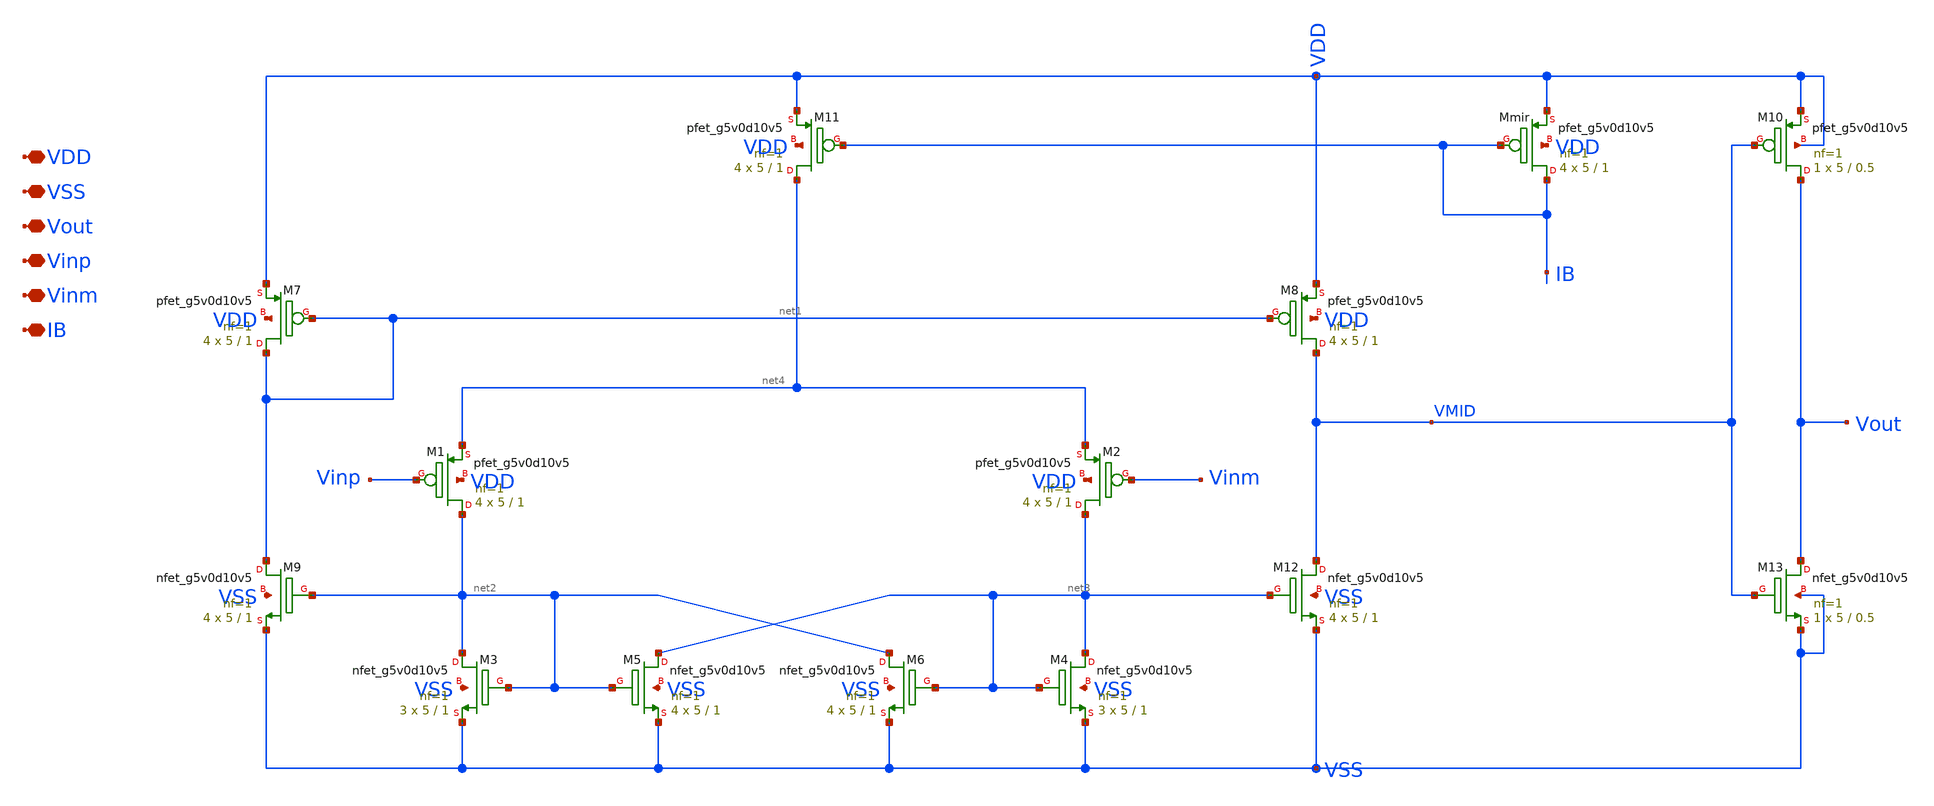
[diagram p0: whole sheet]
** sch_path: design/comparator/comparator_w_obuff.sch
**.subckt comparator_w_obuff VDD VSS Vout Vinp Vinm IB
*.iopin VDD
*.iopin VSS
*.iopin Vout
*.iopin Vinp
*.iopin Vinm
*.iopin IB
XM11 net4 IB VDD VDD sky130_fd_pr__pfet_g5v0d10v5 L=1 W=5 nf=1 ad='int((nf+1)/2) * W/nf * 0.29' as='int((nf+2)/2) * W/nf * 0.29'
+ pd='2*int((nf+1)/2) * (W/nf + 0.29)' ps='2*int((nf+2)/2) * (W/nf + 0.29)' nrd='0.29 / W' nrs='0.29 / W'
+ sa=0 sb=0 sd=0 mult=4 m=4
XM8 VMID net1 VDD VDD sky130_fd_pr__pfet_g5v0d10v5 L=1 W=5 nf=1 ad='int((nf+1)/2) * W/nf * 0.29' as='int((nf+2)/2) * W/nf * 0.29'
+ pd='2*int((nf+1)/2) * (W/nf + 0.29)' ps='2*int((nf+2)/2) * (W/nf + 0.29)' nrd='0.29 / W' nrs='0.29 / W'
+ sa=0 sb=0 sd=0 mult=4 m=4
XM7 net1 net1 VDD VDD sky130_fd_pr__pfet_g5v0d10v5 L=1 W=5 nf=1 ad='int((nf+1)/2) * W/nf * 0.29' as='int((nf+2)/2) * W/nf * 0.29'
+ pd='2*int((nf+1)/2) * (W/nf + 0.29)' ps='2*int((nf+2)/2) * (W/nf + 0.29)' nrd='0.29 / W' nrs='0.29 / W'
+ sa=0 sb=0 sd=0 mult=4 m=4
XM2 net3 Vinm net4 VDD sky130_fd_pr__pfet_g5v0d10v5 L=1 W=5 nf=1 ad='int((nf+1)/2) * W/nf * 0.29' as='int((nf+2)/2) * W/nf * 0.29'
+ pd='2*int((nf+1)/2) * (W/nf + 0.29)' ps='2*int((nf+2)/2) * (W/nf + 0.29)' nrd='0.29 / W' nrs='0.29 / W'
+ sa=0 sb=0 sd=0 mult=4 m=4
XM1 net2 Vinp net4 VDD sky130_fd_pr__pfet_g5v0d10v5 L=1 W=5 nf=1 ad='int((nf+1)/2) * W/nf * 0.29' as='int((nf+2)/2) * W/nf * 0.29'
+ pd='2*int((nf+1)/2) * (W/nf + 0.29)' ps='2*int((nf+2)/2) * (W/nf + 0.29)' nrd='0.29 / W' nrs='0.29 / W'
+ sa=0 sb=0 sd=0 mult=4 m=4
XMmir IB IB VDD VDD sky130_fd_pr__pfet_g5v0d10v5 L=1 W=5 nf=1 ad='int((nf+1)/2) * W/nf * 0.29' as='int((nf+2)/2) * W/nf * 0.29'
+ pd='2*int((nf+1)/2) * (W/nf + 0.29)' ps='2*int((nf+2)/2) * (W/nf + 0.29)' nrd='0.29 / W' nrs='0.29 / W'
+ sa=0 sb=0 sd=0 mult=4 m=4
XM12 VMID net3 VSS VSS sky130_fd_pr__nfet_g5v0d10v5 L=1 W=5 nf=1 ad='int((nf+1)/2) * W/nf * 0.29' as='int((nf+2)/2) * W/nf * 0.29'
+ pd='2*int((nf+1)/2) * (W/nf + 0.29)' ps='2*int((nf+2)/2) * (W/nf + 0.29)' nrd='0.29 / W' nrs='0.29 / W'
+ sa=0 sb=0 sd=0 mult=4 m=4
XM4 net3 net3 VSS VSS sky130_fd_pr__nfet_g5v0d10v5 L=1 W=5 nf=1 ad='int((nf+1)/2) * W/nf * 0.29' as='int((nf+2)/2) * W/nf * 0.29'
+ pd='2*int((nf+1)/2) * (W/nf + 0.29)' ps='2*int((nf+2)/2) * (W/nf + 0.29)' nrd='0.29 / W' nrs='0.29 / W'
+ sa=0 sb=0 sd=0 mult=3 m=3
XM6 net2 net3 VSS VSS sky130_fd_pr__nfet_g5v0d10v5 L=1 W=5 nf=1 ad='int((nf+1)/2) * W/nf * 0.29' as='int((nf+2)/2) * W/nf * 0.29'
+ pd='2*int((nf+1)/2) * (W/nf + 0.29)' ps='2*int((nf+2)/2) * (W/nf + 0.29)' nrd='0.29 / W' nrs='0.29 / W'
+ sa=0 sb=0 sd=0 mult=4 m=4
XM5 net3 net2 VSS VSS sky130_fd_pr__nfet_g5v0d10v5 L=1 W=5 nf=1 ad='int((nf+1)/2) * W/nf * 0.29' as='int((nf+2)/2) * W/nf * 0.29'
+ pd='2*int((nf+1)/2) * (W/nf + 0.29)' ps='2*int((nf+2)/2) * (W/nf + 0.29)' nrd='0.29 / W' nrs='0.29 / W'
+ sa=0 sb=0 sd=0 mult=4 m=4
XM3 net2 net2 VSS VSS sky130_fd_pr__nfet_g5v0d10v5 L=1 W=5 nf=1 ad='int((nf+1)/2) * W/nf * 0.29' as='int((nf+2)/2) * W/nf * 0.29'
+ pd='2*int((nf+1)/2) * (W/nf + 0.29)' ps='2*int((nf+2)/2) * (W/nf + 0.29)' nrd='0.29 / W' nrs='0.29 / W'
+ sa=0 sb=0 sd=0 mult=3 m=3
XM9 net1 net2 VSS VSS sky130_fd_pr__nfet_g5v0d10v5 L=1 W=5 nf=1 ad='int((nf+1)/2) * W/nf * 0.29' as='int((nf+2)/2) * W/nf * 0.29'
+ pd='2*int((nf+1)/2) * (W/nf + 0.29)' ps='2*int((nf+2)/2) * (W/nf + 0.29)' nrd='0.29 / W' nrs='0.29 / W'
+ sa=0 sb=0 sd=0 mult=4 m=4
XM10 Vout VMID VDD VDD sky130_fd_pr__pfet_g5v0d10v5 L=0.5 W=5 nf=1 ad='int((nf+1)/2) * W/nf * 0.29' as='int((nf+2)/2) * W/nf * 0.29'
+ pd='2*int((nf+1)/2) * (W/nf + 0.29)' ps='2*int((nf+2)/2) * (W/nf + 0.29)' nrd='0.29 / W' nrs='0.29 / W'
+ sa=0 sb=0 sd=0 mult=1 m=1
XM13 Vout VMID VSS VSS sky130_fd_pr__nfet_g5v0d10v5 L=0.5 W=5 nf=1 ad='int((nf+1)/2) * W/nf * 0.29' as='int((nf+2)/2) * W/nf * 0.29'
+ pd='2*int((nf+1)/2) * (W/nf + 0.29)' ps='2*int((nf+2)/2) * (W/nf + 0.29)' nrd='0.29 / W' nrs='0.29 / W'
+ sa=0 sb=0 sd=0 mult=1 m=1
**.ends
.end
